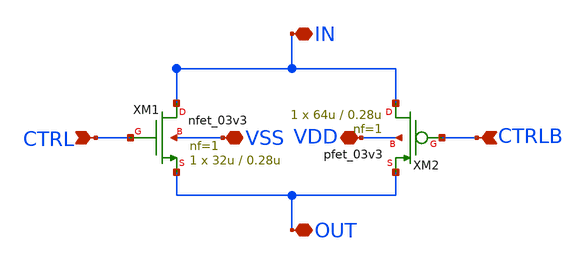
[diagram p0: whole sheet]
** sch_path: designs/libs/core_matchmaker/7D_tg_switch_nmos32u_pmos64u/7D_tg_switch_nmos32u_pmos64u.sch
**.subckt 7D_tg_switch_nmos32u_pmos64u IN OUT VSS VDD CTRL CTRLB
*.iopin IN
*.iopin OUT
*.iopin VSS
*.iopin VDD
*.ipin CTRL
*.ipin CTRLB
XM1 IN CTRL OUT VSS nfet_03v3 L=0.28u W=32u nf=1 ad='int((nf+1)/2) * W/nf * 0.18u' as='int((nf+2)/2) * W/nf * 0.18u'
+ pd='2*int((nf+1)/2) * (W/nf + 0.18u)' ps='2*int((nf+2)/2) * (W/nf + 0.18u)' nrd='0.18u / W' nrs='0.18u / W'
+ sa=0 sb=0 sd=0 m=1
XM2 IN CTRLB OUT VDD pfet_03v3 L=0.28u W=64u nf=1 ad='int((nf+1)/2) * W/nf * 0.18u' as='int((nf+2)/2) * W/nf * 0.18u'
+ pd='2*int((nf+1)/2) * (W/nf + 0.18u)' ps='2*int((nf+2)/2) * (W/nf + 0.18u)' nrd='0.18u / W' nrs='0.18u / W'
+ sa=0 sb=0 sd=0 m=1
**.ends
.end
